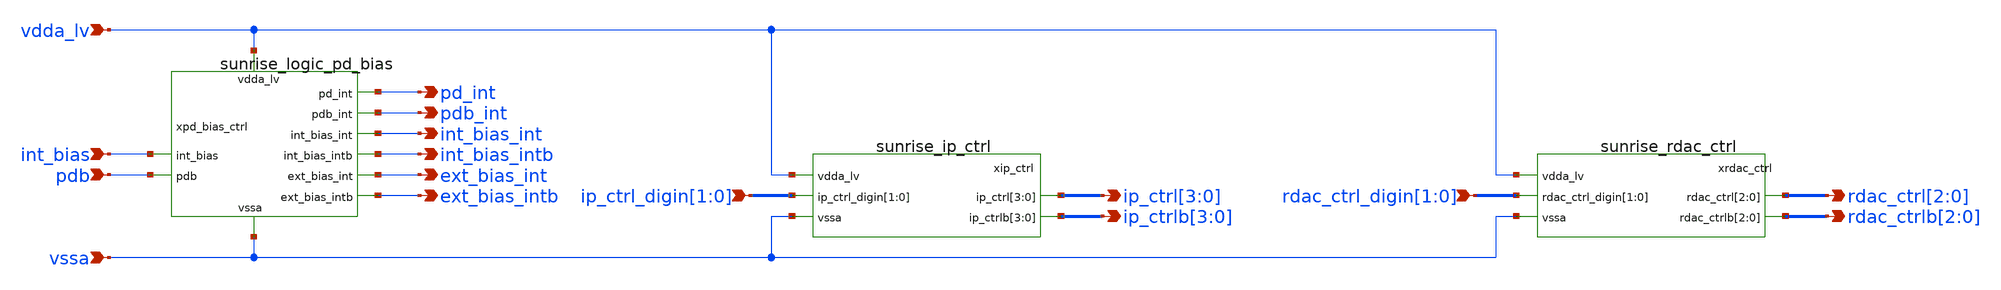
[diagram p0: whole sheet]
** sch_path: Schematics_Layout/sunrise_logic/sunrise_logic.sch
**.subckt sunrise_logic vdda_lv int_bias pdb pd_int pdb_int int_bias_int int_bias_intb ext_bias_int
*+ ext_bias_intb ip_ctrl_digin[1],ip_ctrl_digin[0] ip_ctrl[3],ip_ctrl[2],ip_ctrl[1],ip_ctrl[0]
*+ ip_ctrlb[3],ip_ctrlb[2],ip_ctrlb[1],ip_ctrlb[0] rdac_ctrl_digin[1],rdac_ctrl_digin[0] rdac_ctrl[2],rdac_ctrl[1],rdac_ctrl[0]
*+ rdac_ctrlb[2],rdac_ctrlb[1],rdac_ctrlb[0] vssa
*.ipin vdda_lv
*.ipin int_bias
*.ipin pdb
*.opin pd_int
*.opin pdb_int
*.opin int_bias_int
*.opin int_bias_intb
*.opin ext_bias_int
*.opin ext_bias_intb
*.ipin ip_ctrl_digin[1],ip_ctrl_digin[0]
*.opin ip_ctrl[3],ip_ctrl[2],ip_ctrl[1],ip_ctrl[0]
*.opin ip_ctrlb[3],ip_ctrlb[2],ip_ctrlb[1],ip_ctrlb[0]
*.ipin rdac_ctrl_digin[1],rdac_ctrl_digin[0]
*.opin rdac_ctrl[2],rdac_ctrl[1],rdac_ctrl[0]
*.opin rdac_ctrlb[2],rdac_ctrlb[1],rdac_ctrlb[0]
*.ipin vssa
xip_ctrl ip_ctrl_digin[1] ip_ctrl_digin[0] ip_ctrl[3] ip_ctrl[2] ip_ctrl[1] ip_ctrl[0] vdda_lv vssa
+ ip_ctrlb[3] ip_ctrlb[2] ip_ctrlb[1] ip_ctrlb[0] sunrise_ip_ctrl
xrdac_ctrl rdac_ctrl_digin[1] rdac_ctrl_digin[0] rdac_ctrl[2] rdac_ctrl[1] rdac_ctrl[0] vdda_lv vssa
+ rdac_ctrlb[2] rdac_ctrlb[1] rdac_ctrlb[0] sunrise_rdac_ctrl
xpd_bias_ctrl vdda_lv vssa int_bias_intb int_bias int_bias_int pdb ext_bias_intb ext_bias_int
+ pdb_int pd_int sunrise_logic_pd_bias
**.ends
.end
